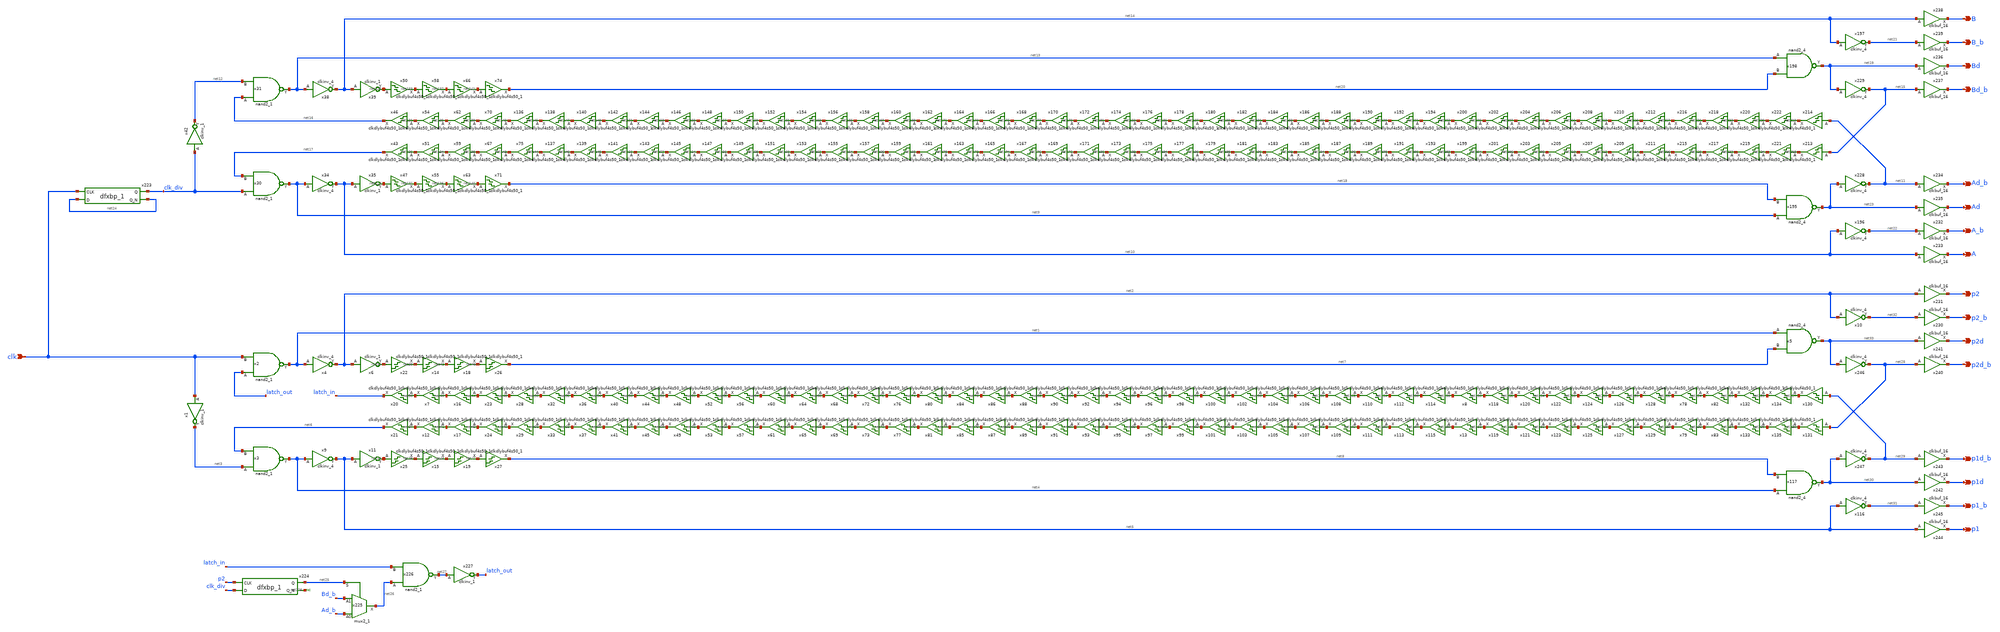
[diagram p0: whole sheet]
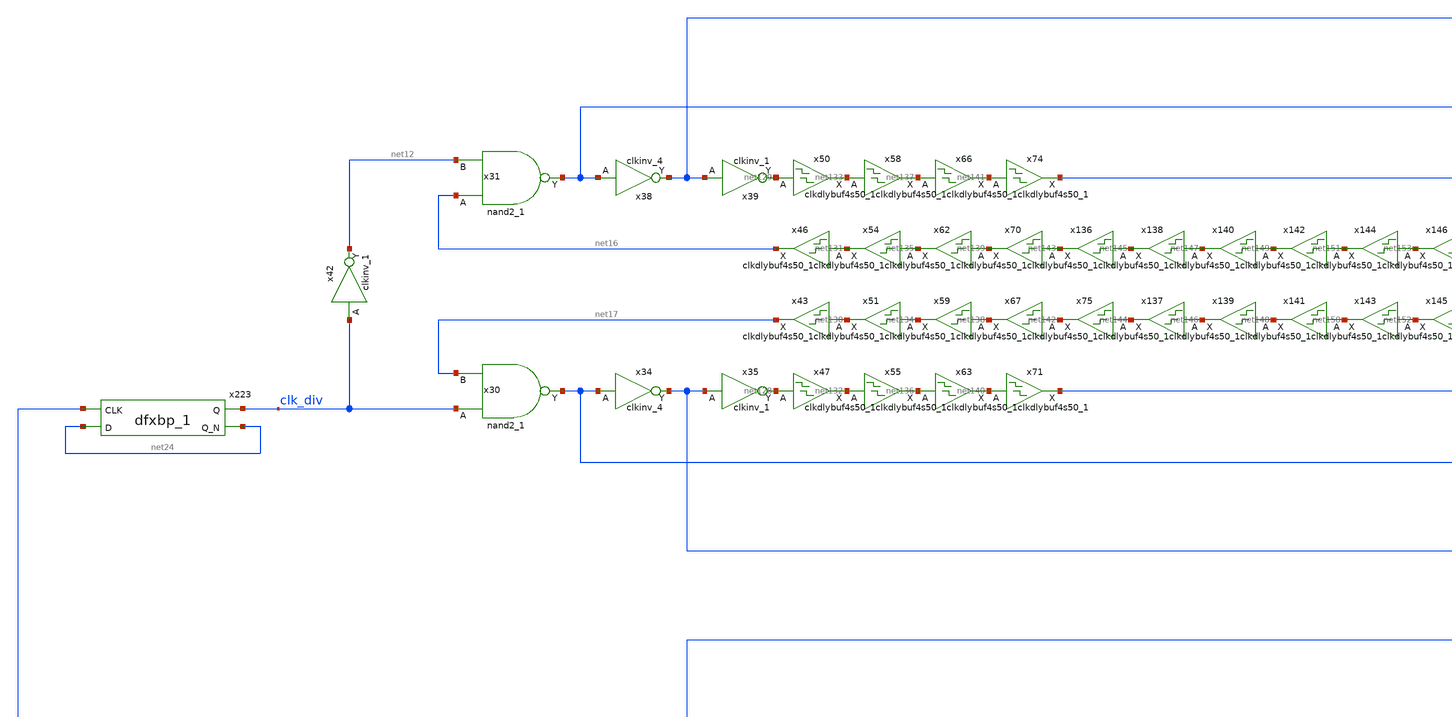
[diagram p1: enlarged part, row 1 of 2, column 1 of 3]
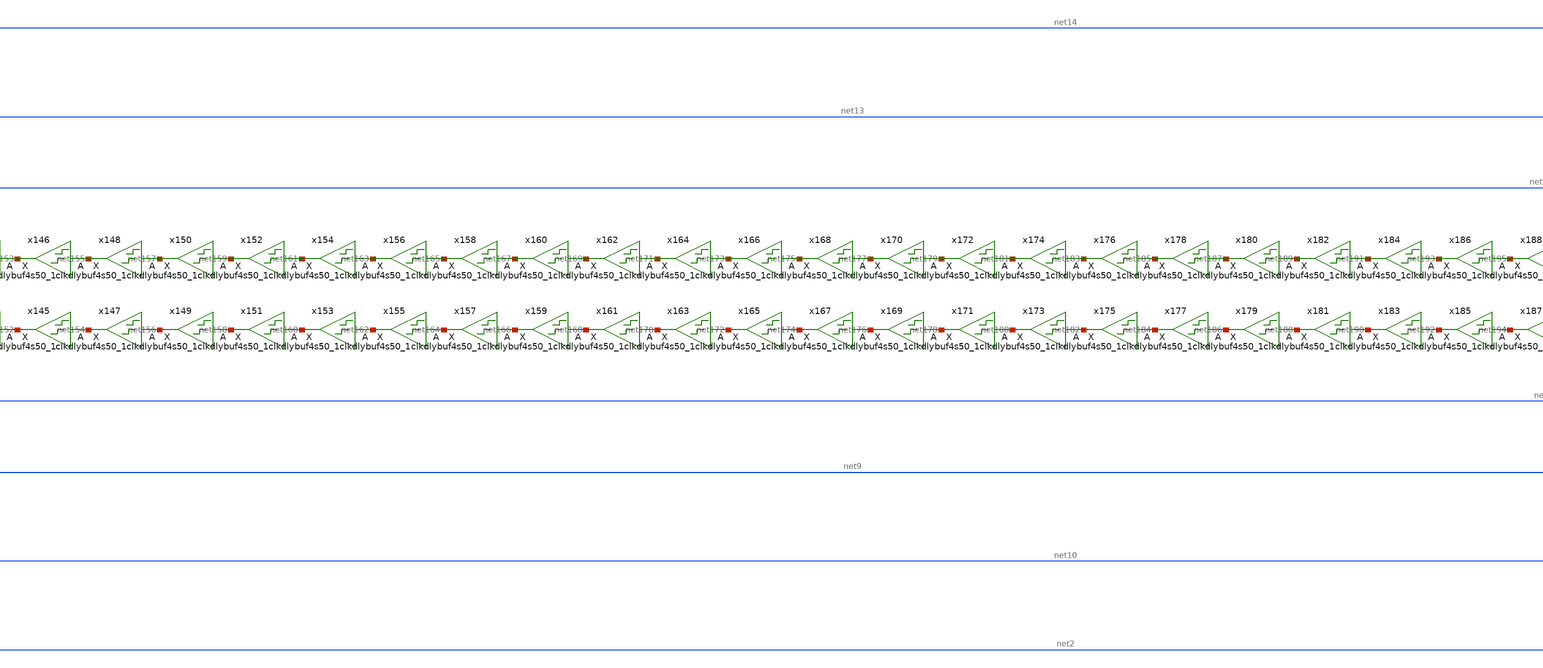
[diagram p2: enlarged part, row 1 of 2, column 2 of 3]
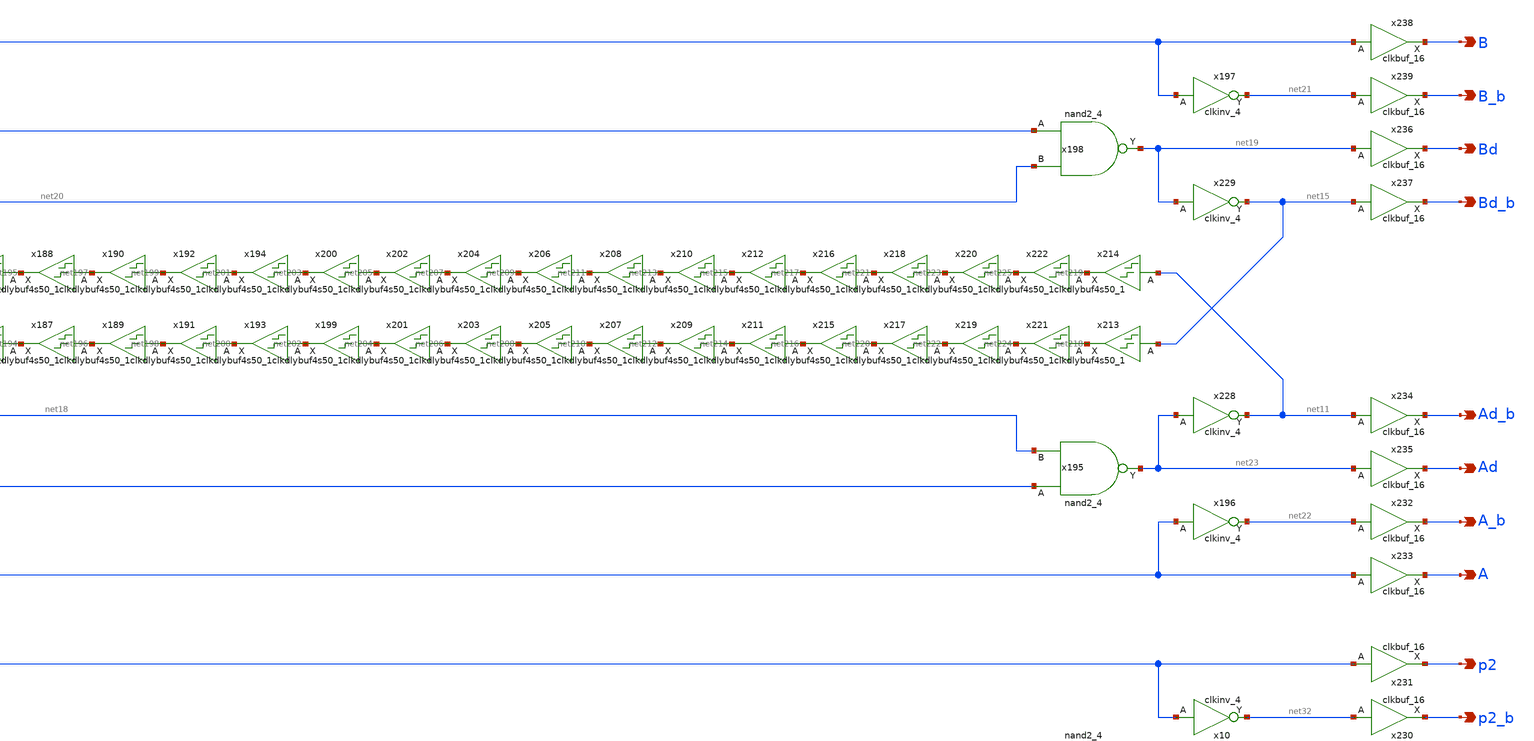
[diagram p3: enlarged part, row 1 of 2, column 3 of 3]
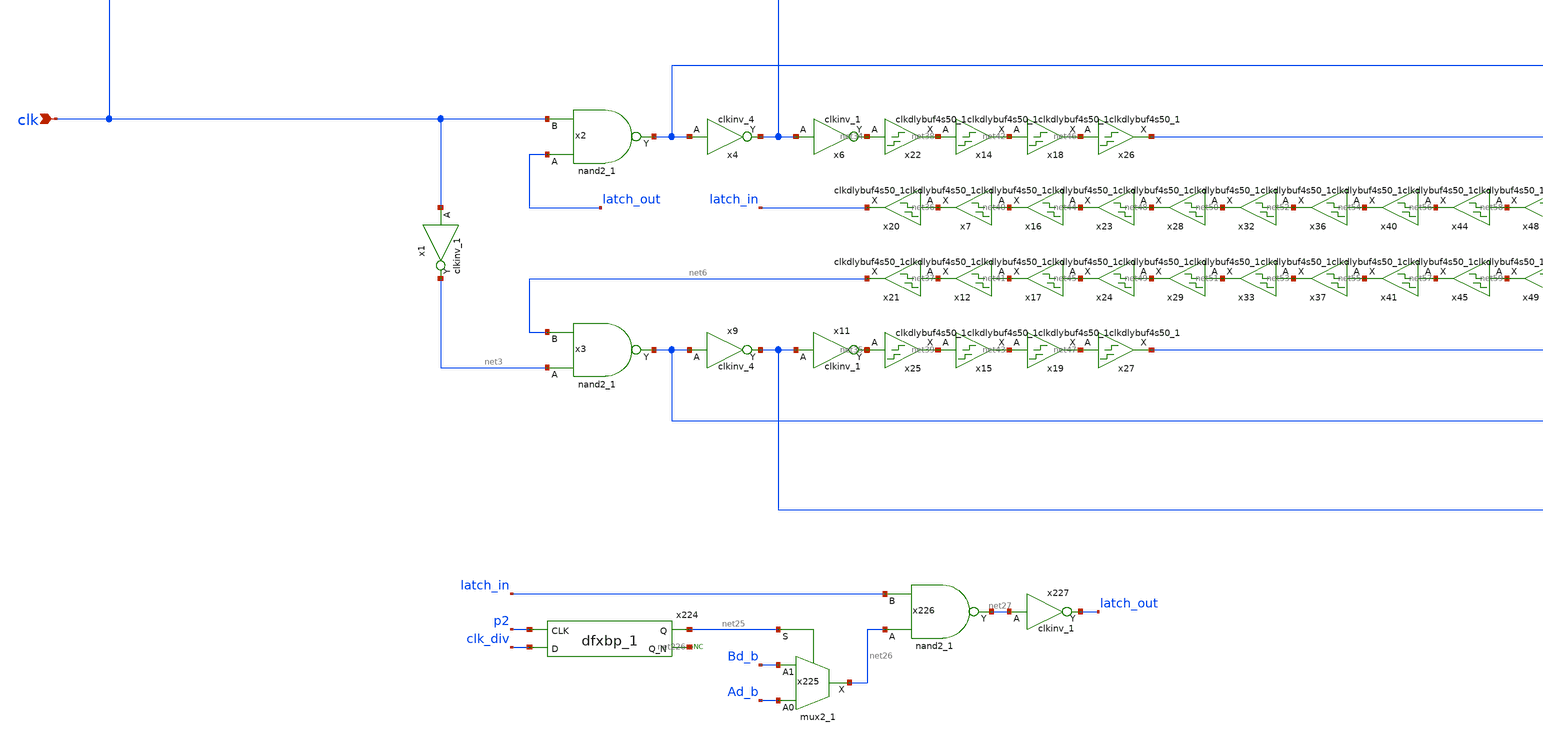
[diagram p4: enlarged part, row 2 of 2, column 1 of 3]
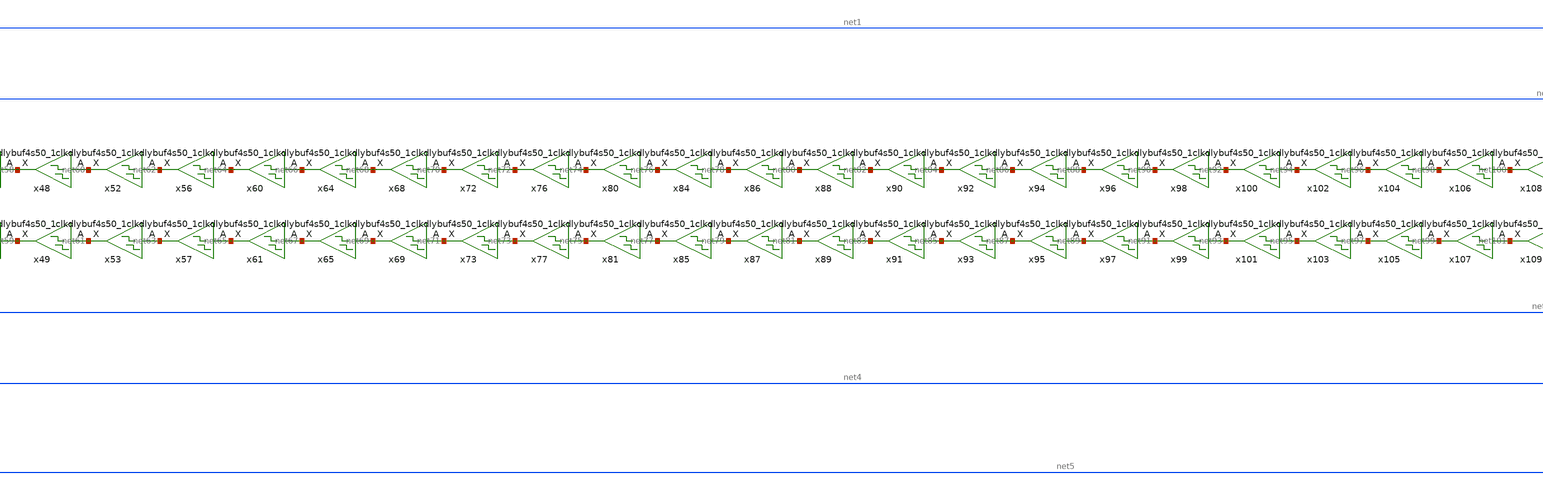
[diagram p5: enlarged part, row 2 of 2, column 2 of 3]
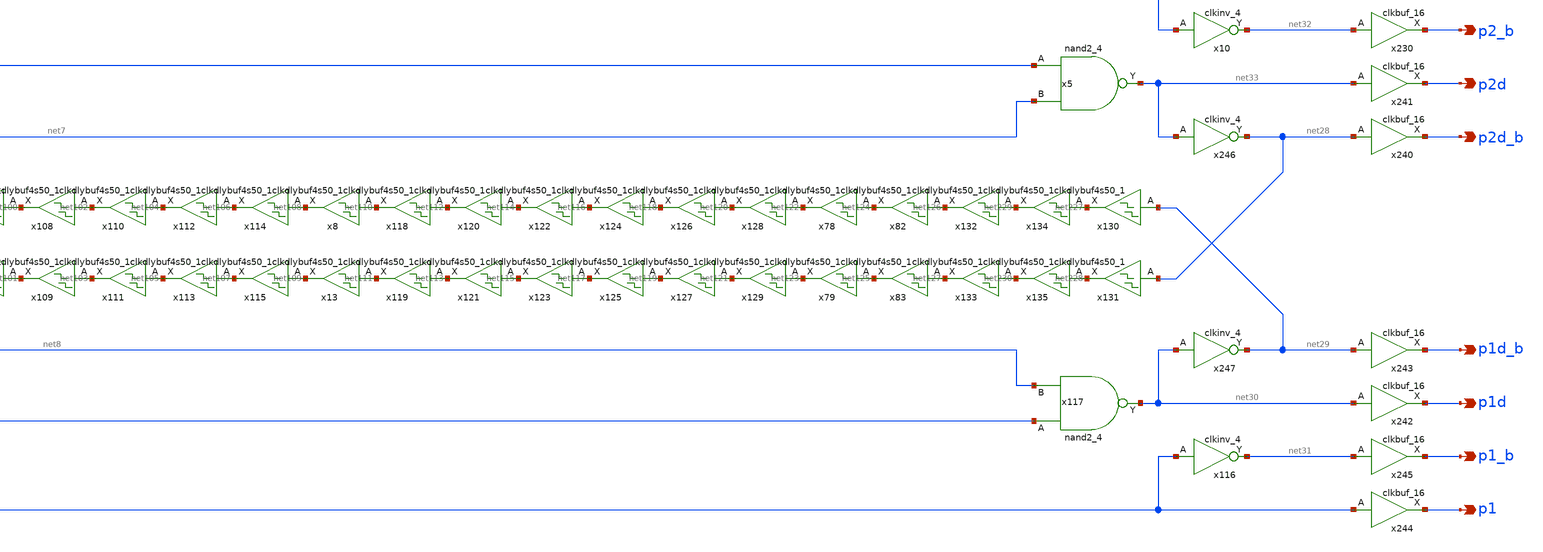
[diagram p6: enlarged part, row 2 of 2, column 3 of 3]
** sch_path: design/analog_modulator/schematic/clock.sch
**.subckt clock clk p2d_b p2d p2_b p2 p1d_b p1d p1_b p1 Ad_b Ad A_b A Bd_b Bd B_b B
*.ipin clk
*.opin p2d_b
*.opin p2d
*.opin p2_b
*.opin p2
*.opin p1d_b
*.opin p1d
*.opin p1_b
*.opin p1
*.opin Ad_b
*.opin Ad
*.opin A_b
*.opin A
*.opin Bd_b
*.opin Bd
*.opin B_b
*.opin B
x2 latch_out clk VSS VSS VDD VDD net1 sky130_fd_sc_hd__nand2_1
x3 net3 net6 VSS VSS VDD VDD net4 sky130_fd_sc_hd__nand2_1
x4 net1 VSS VSS VDD VDD net2 sky130_fd_sc_hd__clkinv_4
x6 net2 VSS VSS VDD VDD net34 sky130_fd_sc_hd__clkinv_1
x9 net4 VSS VSS VDD VDD net5 sky130_fd_sc_hd__clkinv_4
x11 net5 VSS VSS VDD VDD net35 sky130_fd_sc_hd__clkinv_1
x1 clk VSS VSS VDD VDD net3 sky130_fd_sc_hd__clkinv_1
x20 net36 VSS VSS VDD VDD latch_in sky130_fd_sc_hd__clkdlybuf4s50_1
x21 net37 VSS VSS VDD VDD net6 sky130_fd_sc_hd__clkdlybuf4s50_1
x22 net34 VSS VSS VDD VDD net38 sky130_fd_sc_hd__clkdlybuf4s50_1
x25 net35 VSS VSS VDD VDD net39 sky130_fd_sc_hd__clkdlybuf4s50_1
x7 net40 VSS VSS VDD VDD net36 sky130_fd_sc_hd__clkdlybuf4s50_1
x12 net41 VSS VSS VDD VDD net37 sky130_fd_sc_hd__clkdlybuf4s50_1
x14 net38 VSS VSS VDD VDD net42 sky130_fd_sc_hd__clkdlybuf4s50_1
x15 net39 VSS VSS VDD VDD net43 sky130_fd_sc_hd__clkdlybuf4s50_1
x16 net44 VSS VSS VDD VDD net40 sky130_fd_sc_hd__clkdlybuf4s50_1
x17 net45 VSS VSS VDD VDD net41 sky130_fd_sc_hd__clkdlybuf4s50_1
x18 net42 VSS VSS VDD VDD net46 sky130_fd_sc_hd__clkdlybuf4s50_1
x19 net43 VSS VSS VDD VDD net47 sky130_fd_sc_hd__clkdlybuf4s50_1
x23 net48 VSS VSS VDD VDD net44 sky130_fd_sc_hd__clkdlybuf4s50_1
x24 net49 VSS VSS VDD VDD net45 sky130_fd_sc_hd__clkdlybuf4s50_1
x26 net46 VSS VSS VDD VDD net7 sky130_fd_sc_hd__clkdlybuf4s50_1
x27 net47 VSS VSS VDD VDD net8 sky130_fd_sc_hd__clkdlybuf4s50_1
x28 net50 VSS VSS VDD VDD net48 sky130_fd_sc_hd__clkdlybuf4s50_1
x29 net51 VSS VSS VDD VDD net49 sky130_fd_sc_hd__clkdlybuf4s50_1
x32 net52 VSS VSS VDD VDD net50 sky130_fd_sc_hd__clkdlybuf4s50_1
x33 net53 VSS VSS VDD VDD net51 sky130_fd_sc_hd__clkdlybuf4s50_1
x36 net54 VSS VSS VDD VDD net52 sky130_fd_sc_hd__clkdlybuf4s50_1
x37 net55 VSS VSS VDD VDD net53 sky130_fd_sc_hd__clkdlybuf4s50_1
x40 net56 VSS VSS VDD VDD net54 sky130_fd_sc_hd__clkdlybuf4s50_1
x41 net57 VSS VSS VDD VDD net55 sky130_fd_sc_hd__clkdlybuf4s50_1
x44 net58 VSS VSS VDD VDD net56 sky130_fd_sc_hd__clkdlybuf4s50_1
x45 net59 VSS VSS VDD VDD net57 sky130_fd_sc_hd__clkdlybuf4s50_1
x48 net60 VSS VSS VDD VDD net58 sky130_fd_sc_hd__clkdlybuf4s50_1
x49 net61 VSS VSS VDD VDD net59 sky130_fd_sc_hd__clkdlybuf4s50_1
x52 net62 VSS VSS VDD VDD net60 sky130_fd_sc_hd__clkdlybuf4s50_1
x53 net63 VSS VSS VDD VDD net61 sky130_fd_sc_hd__clkdlybuf4s50_1
x56 net64 VSS VSS VDD VDD net62 sky130_fd_sc_hd__clkdlybuf4s50_1
x57 net65 VSS VSS VDD VDD net63 sky130_fd_sc_hd__clkdlybuf4s50_1
x60 net66 VSS VSS VDD VDD net64 sky130_fd_sc_hd__clkdlybuf4s50_1
x61 net67 VSS VSS VDD VDD net65 sky130_fd_sc_hd__clkdlybuf4s50_1
x64 net68 VSS VSS VDD VDD net66 sky130_fd_sc_hd__clkdlybuf4s50_1
x65 net69 VSS VSS VDD VDD net67 sky130_fd_sc_hd__clkdlybuf4s50_1
x68 net70 VSS VSS VDD VDD net68 sky130_fd_sc_hd__clkdlybuf4s50_1
x69 net71 VSS VSS VDD VDD net69 sky130_fd_sc_hd__clkdlybuf4s50_1
x72 net72 VSS VSS VDD VDD net70 sky130_fd_sc_hd__clkdlybuf4s50_1
x73 net73 VSS VSS VDD VDD net71 sky130_fd_sc_hd__clkdlybuf4s50_1
x76 net74 VSS VSS VDD VDD net72 sky130_fd_sc_hd__clkdlybuf4s50_1
x77 net75 VSS VSS VDD VDD net73 sky130_fd_sc_hd__clkdlybuf4s50_1
x80 net76 VSS VSS VDD VDD net74 sky130_fd_sc_hd__clkdlybuf4s50_1
x81 net77 VSS VSS VDD VDD net75 sky130_fd_sc_hd__clkdlybuf4s50_1
x84 net78 VSS VSS VDD VDD net76 sky130_fd_sc_hd__clkdlybuf4s50_1
x85 net79 VSS VSS VDD VDD net77 sky130_fd_sc_hd__clkdlybuf4s50_1
x86 net80 VSS VSS VDD VDD net78 sky130_fd_sc_hd__clkdlybuf4s50_1
x87 net81 VSS VSS VDD VDD net79 sky130_fd_sc_hd__clkdlybuf4s50_1
x88 net82 VSS VSS VDD VDD net80 sky130_fd_sc_hd__clkdlybuf4s50_1
x89 net83 VSS VSS VDD VDD net81 sky130_fd_sc_hd__clkdlybuf4s50_1
x90 net84 VSS VSS VDD VDD net82 sky130_fd_sc_hd__clkdlybuf4s50_1
x91 net85 VSS VSS VDD VDD net83 sky130_fd_sc_hd__clkdlybuf4s50_1
x92 net86 VSS VSS VDD VDD net84 sky130_fd_sc_hd__clkdlybuf4s50_1
x93 net87 VSS VSS VDD VDD net85 sky130_fd_sc_hd__clkdlybuf4s50_1
x94 net88 VSS VSS VDD VDD net86 sky130_fd_sc_hd__clkdlybuf4s50_1
x95 net89 VSS VSS VDD VDD net87 sky130_fd_sc_hd__clkdlybuf4s50_1
x96 net90 VSS VSS VDD VDD net88 sky130_fd_sc_hd__clkdlybuf4s50_1
x97 net91 VSS VSS VDD VDD net89 sky130_fd_sc_hd__clkdlybuf4s50_1
x98 net92 VSS VSS VDD VDD net90 sky130_fd_sc_hd__clkdlybuf4s50_1
x99 net93 VSS VSS VDD VDD net91 sky130_fd_sc_hd__clkdlybuf4s50_1
x100 net94 VSS VSS VDD VDD net92 sky130_fd_sc_hd__clkdlybuf4s50_1
x101 net95 VSS VSS VDD VDD net93 sky130_fd_sc_hd__clkdlybuf4s50_1
x102 net96 VSS VSS VDD VDD net94 sky130_fd_sc_hd__clkdlybuf4s50_1
x103 net97 VSS VSS VDD VDD net95 sky130_fd_sc_hd__clkdlybuf4s50_1
x104 net98 VSS VSS VDD VDD net96 sky130_fd_sc_hd__clkdlybuf4s50_1
x105 net99 VSS VSS VDD VDD net97 sky130_fd_sc_hd__clkdlybuf4s50_1
x106 net100 VSS VSS VDD VDD net98 sky130_fd_sc_hd__clkdlybuf4s50_1
x107 net101 VSS VSS VDD VDD net99 sky130_fd_sc_hd__clkdlybuf4s50_1
x108 net102 VSS VSS VDD VDD net100 sky130_fd_sc_hd__clkdlybuf4s50_1
x109 net103 VSS VSS VDD VDD net101 sky130_fd_sc_hd__clkdlybuf4s50_1
x110 net104 VSS VSS VDD VDD net102 sky130_fd_sc_hd__clkdlybuf4s50_1
x111 net105 VSS VSS VDD VDD net103 sky130_fd_sc_hd__clkdlybuf4s50_1
x112 net106 VSS VSS VDD VDD net104 sky130_fd_sc_hd__clkdlybuf4s50_1
x113 net107 VSS VSS VDD VDD net105 sky130_fd_sc_hd__clkdlybuf4s50_1
x114 net108 VSS VSS VDD VDD net106 sky130_fd_sc_hd__clkdlybuf4s50_1
x115 net109 VSS VSS VDD VDD net107 sky130_fd_sc_hd__clkdlybuf4s50_1
x8 net110 VSS VSS VDD VDD net108 sky130_fd_sc_hd__clkdlybuf4s50_1
x13 net111 VSS VSS VDD VDD net109 sky130_fd_sc_hd__clkdlybuf4s50_1
x118 net112 VSS VSS VDD VDD net110 sky130_fd_sc_hd__clkdlybuf4s50_1
x119 net113 VSS VSS VDD VDD net111 sky130_fd_sc_hd__clkdlybuf4s50_1
x120 net114 VSS VSS VDD VDD net112 sky130_fd_sc_hd__clkdlybuf4s50_1
x121 net115 VSS VSS VDD VDD net113 sky130_fd_sc_hd__clkdlybuf4s50_1
x122 net116 VSS VSS VDD VDD net114 sky130_fd_sc_hd__clkdlybuf4s50_1
x123 net117 VSS VSS VDD VDD net115 sky130_fd_sc_hd__clkdlybuf4s50_1
x124 net118 VSS VSS VDD VDD net116 sky130_fd_sc_hd__clkdlybuf4s50_1
x125 net119 VSS VSS VDD VDD net117 sky130_fd_sc_hd__clkdlybuf4s50_1
x126 net120 VSS VSS VDD VDD net118 sky130_fd_sc_hd__clkdlybuf4s50_1
x127 net121 VSS VSS VDD VDD net119 sky130_fd_sc_hd__clkdlybuf4s50_1
x128 net122 VSS VSS VDD VDD net120 sky130_fd_sc_hd__clkdlybuf4s50_1
x129 net123 VSS VSS VDD VDD net121 sky130_fd_sc_hd__clkdlybuf4s50_1
x78 net124 VSS VSS VDD VDD net122 sky130_fd_sc_hd__clkdlybuf4s50_1
x79 net125 VSS VSS VDD VDD net123 sky130_fd_sc_hd__clkdlybuf4s50_1
x82 net126 VSS VSS VDD VDD net124 sky130_fd_sc_hd__clkdlybuf4s50_1
x83 net127 VSS VSS VDD VDD net125 sky130_fd_sc_hd__clkdlybuf4s50_1
x30 clk_div net17 VSS VSS VDD VDD net9 sky130_fd_sc_hd__nand2_1
x31 net16 net12 VSS VSS VDD VDD net13 sky130_fd_sc_hd__nand2_1
x34 net9 VSS VSS VDD VDD net10 sky130_fd_sc_hd__clkinv_4
x35 net10 VSS VSS VDD VDD net128 sky130_fd_sc_hd__clkinv_1
x38 net13 VSS VSS VDD VDD net14 sky130_fd_sc_hd__clkinv_4
x39 net14 VSS VSS VDD VDD net129 sky130_fd_sc_hd__clkinv_1
x42 clk_div VSS VSS VDD VDD net12 sky130_fd_sc_hd__clkinv_1
x43 net130 VSS VSS VDD VDD net17 sky130_fd_sc_hd__clkdlybuf4s50_1
x46 net131 VSS VSS VDD VDD net16 sky130_fd_sc_hd__clkdlybuf4s50_1
x47 net128 VSS VSS VDD VDD net132 sky130_fd_sc_hd__clkdlybuf4s50_1
x50 net129 VSS VSS VDD VDD net133 sky130_fd_sc_hd__clkdlybuf4s50_1
x51 net134 VSS VSS VDD VDD net130 sky130_fd_sc_hd__clkdlybuf4s50_1
x54 net135 VSS VSS VDD VDD net131 sky130_fd_sc_hd__clkdlybuf4s50_1
x55 net132 VSS VSS VDD VDD net136 sky130_fd_sc_hd__clkdlybuf4s50_1
x58 net133 VSS VSS VDD VDD net137 sky130_fd_sc_hd__clkdlybuf4s50_1
x59 net138 VSS VSS VDD VDD net134 sky130_fd_sc_hd__clkdlybuf4s50_1
x62 net139 VSS VSS VDD VDD net135 sky130_fd_sc_hd__clkdlybuf4s50_1
x63 net136 VSS VSS VDD VDD net140 sky130_fd_sc_hd__clkdlybuf4s50_1
x66 net137 VSS VSS VDD VDD net141 sky130_fd_sc_hd__clkdlybuf4s50_1
x67 net142 VSS VSS VDD VDD net138 sky130_fd_sc_hd__clkdlybuf4s50_1
x70 net143 VSS VSS VDD VDD net139 sky130_fd_sc_hd__clkdlybuf4s50_1
x71 net140 VSS VSS VDD VDD net18 sky130_fd_sc_hd__clkdlybuf4s50_1
x74 net141 VSS VSS VDD VDD net20 sky130_fd_sc_hd__clkdlybuf4s50_1
x75 net144 VSS VSS VDD VDD net142 sky130_fd_sc_hd__clkdlybuf4s50_1
x136 net145 VSS VSS VDD VDD net143 sky130_fd_sc_hd__clkdlybuf4s50_1
x137 net146 VSS VSS VDD VDD net144 sky130_fd_sc_hd__clkdlybuf4s50_1
x138 net147 VSS VSS VDD VDD net145 sky130_fd_sc_hd__clkdlybuf4s50_1
x139 net148 VSS VSS VDD VDD net146 sky130_fd_sc_hd__clkdlybuf4s50_1
x140 net149 VSS VSS VDD VDD net147 sky130_fd_sc_hd__clkdlybuf4s50_1
x141 net150 VSS VSS VDD VDD net148 sky130_fd_sc_hd__clkdlybuf4s50_1
x142 net151 VSS VSS VDD VDD net149 sky130_fd_sc_hd__clkdlybuf4s50_1
x143 net152 VSS VSS VDD VDD net150 sky130_fd_sc_hd__clkdlybuf4s50_1
x144 net153 VSS VSS VDD VDD net151 sky130_fd_sc_hd__clkdlybuf4s50_1
x145 net154 VSS VSS VDD VDD net152 sky130_fd_sc_hd__clkdlybuf4s50_1
x146 net155 VSS VSS VDD VDD net153 sky130_fd_sc_hd__clkdlybuf4s50_1
x147 net156 VSS VSS VDD VDD net154 sky130_fd_sc_hd__clkdlybuf4s50_1
x148 net157 VSS VSS VDD VDD net155 sky130_fd_sc_hd__clkdlybuf4s50_1
x149 net158 VSS VSS VDD VDD net156 sky130_fd_sc_hd__clkdlybuf4s50_1
x150 net159 VSS VSS VDD VDD net157 sky130_fd_sc_hd__clkdlybuf4s50_1
x151 net160 VSS VSS VDD VDD net158 sky130_fd_sc_hd__clkdlybuf4s50_1
x152 net161 VSS VSS VDD VDD net159 sky130_fd_sc_hd__clkdlybuf4s50_1
x153 net162 VSS VSS VDD VDD net160 sky130_fd_sc_hd__clkdlybuf4s50_1
x154 net163 VSS VSS VDD VDD net161 sky130_fd_sc_hd__clkdlybuf4s50_1
x155 net164 VSS VSS VDD VDD net162 sky130_fd_sc_hd__clkdlybuf4s50_1
x156 net165 VSS VSS VDD VDD net163 sky130_fd_sc_hd__clkdlybuf4s50_1
x157 net166 VSS VSS VDD VDD net164 sky130_fd_sc_hd__clkdlybuf4s50_1
x158 net167 VSS VSS VDD VDD net165 sky130_fd_sc_hd__clkdlybuf4s50_1
x159 net168 VSS VSS VDD VDD net166 sky130_fd_sc_hd__clkdlybuf4s50_1
x160 net169 VSS VSS VDD VDD net167 sky130_fd_sc_hd__clkdlybuf4s50_1
x161 net170 VSS VSS VDD VDD net168 sky130_fd_sc_hd__clkdlybuf4s50_1
x162 net171 VSS VSS VDD VDD net169 sky130_fd_sc_hd__clkdlybuf4s50_1
x163 net172 VSS VSS VDD VDD net170 sky130_fd_sc_hd__clkdlybuf4s50_1
x164 net173 VSS VSS VDD VDD net171 sky130_fd_sc_hd__clkdlybuf4s50_1
x165 net174 VSS VSS VDD VDD net172 sky130_fd_sc_hd__clkdlybuf4s50_1
x166 net175 VSS VSS VDD VDD net173 sky130_fd_sc_hd__clkdlybuf4s50_1
x167 net176 VSS VSS VDD VDD net174 sky130_fd_sc_hd__clkdlybuf4s50_1
x168 net177 VSS VSS VDD VDD net175 sky130_fd_sc_hd__clkdlybuf4s50_1
x169 net178 VSS VSS VDD VDD net176 sky130_fd_sc_hd__clkdlybuf4s50_1
x170 net179 VSS VSS VDD VDD net177 sky130_fd_sc_hd__clkdlybuf4s50_1
x171 net180 VSS VSS VDD VDD net178 sky130_fd_sc_hd__clkdlybuf4s50_1
x172 net181 VSS VSS VDD VDD net179 sky130_fd_sc_hd__clkdlybuf4s50_1
x173 net182 VSS VSS VDD VDD net180 sky130_fd_sc_hd__clkdlybuf4s50_1
x174 net183 VSS VSS VDD VDD net181 sky130_fd_sc_hd__clkdlybuf4s50_1
x175 net184 VSS VSS VDD VDD net182 sky130_fd_sc_hd__clkdlybuf4s50_1
x176 net185 VSS VSS VDD VDD net183 sky130_fd_sc_hd__clkdlybuf4s50_1
x177 net186 VSS VSS VDD VDD net184 sky130_fd_sc_hd__clkdlybuf4s50_1
x178 net187 VSS VSS VDD VDD net185 sky130_fd_sc_hd__clkdlybuf4s50_1
x179 net188 VSS VSS VDD VDD net186 sky130_fd_sc_hd__clkdlybuf4s50_1
x180 net189 VSS VSS VDD VDD net187 sky130_fd_sc_hd__clkdlybuf4s50_1
x181 net190 VSS VSS VDD VDD net188 sky130_fd_sc_hd__clkdlybuf4s50_1
x182 net191 VSS VSS VDD VDD net189 sky130_fd_sc_hd__clkdlybuf4s50_1
x183 net192 VSS VSS VDD VDD net190 sky130_fd_sc_hd__clkdlybuf4s50_1
x184 net193 VSS VSS VDD VDD net191 sky130_fd_sc_hd__clkdlybuf4s50_1
x185 net194 VSS VSS VDD VDD net192 sky130_fd_sc_hd__clkdlybuf4s50_1
x186 net195 VSS VSS VDD VDD net193 sky130_fd_sc_hd__clkdlybuf4s50_1
x187 net196 VSS VSS VDD VDD net194 sky130_fd_sc_hd__clkdlybuf4s50_1
x188 net197 VSS VSS VDD VDD net195 sky130_fd_sc_hd__clkdlybuf4s50_1
x189 net198 VSS VSS VDD VDD net196 sky130_fd_sc_hd__clkdlybuf4s50_1
x190 net199 VSS VSS VDD VDD net197 sky130_fd_sc_hd__clkdlybuf4s50_1
x191 net200 VSS VSS VDD VDD net198 sky130_fd_sc_hd__clkdlybuf4s50_1
x192 net201 VSS VSS VDD VDD net199 sky130_fd_sc_hd__clkdlybuf4s50_1
x193 net202 VSS VSS VDD VDD net200 sky130_fd_sc_hd__clkdlybuf4s50_1
x194 net203 VSS VSS VDD VDD net201 sky130_fd_sc_hd__clkdlybuf4s50_1
x195 net9 net18 VSS VSS VDD VDD net23 sky130_fd_sc_hd__nand2_4
x196 net10 VSS VSS VDD VDD net22 sky130_fd_sc_hd__clkinv_4
x197 net14 VSS VSS VDD VDD net21 sky130_fd_sc_hd__clkinv_4
x198 net13 net20 VSS VSS VDD VDD net19 sky130_fd_sc_hd__nand2_4
x199 net204 VSS VSS VDD VDD net202 sky130_fd_sc_hd__clkdlybuf4s50_1
x200 net205 VSS VSS VDD VDD net203 sky130_fd_sc_hd__clkdlybuf4s50_1
x201 net206 VSS VSS VDD VDD net204 sky130_fd_sc_hd__clkdlybuf4s50_1
x202 net207 VSS VSS VDD VDD net205 sky130_fd_sc_hd__clkdlybuf4s50_1
x203 net208 VSS VSS VDD VDD net206 sky130_fd_sc_hd__clkdlybuf4s50_1
x204 net209 VSS VSS VDD VDD net207 sky130_fd_sc_hd__clkdlybuf4s50_1
x205 net210 VSS VSS VDD VDD net208 sky130_fd_sc_hd__clkdlybuf4s50_1
x206 net211 VSS VSS VDD VDD net209 sky130_fd_sc_hd__clkdlybuf4s50_1
x207 net212 VSS VSS VDD VDD net210 sky130_fd_sc_hd__clkdlybuf4s50_1
x208 net213 VSS VSS VDD VDD net211 sky130_fd_sc_hd__clkdlybuf4s50_1
x209 net214 VSS VSS VDD VDD net212 sky130_fd_sc_hd__clkdlybuf4s50_1
x210 net215 VSS VSS VDD VDD net213 sky130_fd_sc_hd__clkdlybuf4s50_1
x211 net216 VSS VSS VDD VDD net214 sky130_fd_sc_hd__clkdlybuf4s50_1
x212 net217 VSS VSS VDD VDD net215 sky130_fd_sc_hd__clkdlybuf4s50_1
x213 net15 VSS VSS VDD VDD net218 sky130_fd_sc_hd__clkdlybuf4s50_1
x214 net11 VSS VSS VDD VDD net219 sky130_fd_sc_hd__clkdlybuf4s50_1
x215 net220 VSS VSS VDD VDD net216 sky130_fd_sc_hd__clkdlybuf4s50_1
x216 net221 VSS VSS VDD VDD net217 sky130_fd_sc_hd__clkdlybuf4s50_1
x217 net222 VSS VSS VDD VDD net220 sky130_fd_sc_hd__clkdlybuf4s50_1
x218 net223 VSS VSS VDD VDD net221 sky130_fd_sc_hd__clkdlybuf4s50_1
x219 net224 VSS VSS VDD VDD net222 sky130_fd_sc_hd__clkdlybuf4s50_1
x220 net225 VSS VSS VDD VDD net223 sky130_fd_sc_hd__clkdlybuf4s50_1
x221 net218 VSS VSS VDD VDD net224 sky130_fd_sc_hd__clkdlybuf4s50_1
x222 net219 VSS VSS VDD VDD net225 sky130_fd_sc_hd__clkdlybuf4s50_1
x223 clk net24 VSS VSS VDD VDD clk_div net24 sky130_fd_sc_hd__dfxbp_1
x224 p2 clk_div VSS VSS VDD VDD net25 net226 sky130_fd_sc_hd__dfxbp_1
x225 Ad_b Bd_b net25 VSS VSS VDD VDD net26 sky130_fd_sc_hd__mux2_1
x226 net26 latch_in VSS VSS VDD VDD net27 sky130_fd_sc_hd__nand2_1
x227 net27 VSS VSS VDD VDD latch_out sky130_fd_sc_hd__clkinv_1
* noconn #net226
x232 net22 VSS VSS VDD VDD A_b sky130_fd_sc_hd__clkbuf_16
x233 net10 VSS VSS VDD VDD A sky130_fd_sc_hd__clkbuf_16
x234 net11 VSS VSS VDD VDD Ad_b sky130_fd_sc_hd__clkbuf_16
x235 net23 VSS VSS VDD VDD Ad sky130_fd_sc_hd__clkbuf_16
x236 net19 VSS VSS VDD VDD Bd sky130_fd_sc_hd__clkbuf_16
x237 net15 VSS VSS VDD VDD Bd_b sky130_fd_sc_hd__clkbuf_16
x238 net14 VSS VSS VDD VDD B sky130_fd_sc_hd__clkbuf_16
x239 net21 VSS VSS VDD VDD B_b sky130_fd_sc_hd__clkbuf_16
x228 net23 VSS VSS VDD VDD net11 sky130_fd_sc_hd__clkinv_4
x229 net19 VSS VSS VDD VDD net15 sky130_fd_sc_hd__clkinv_4
x5 net1 net7 VSS VSS VDD VDD net33 sky130_fd_sc_hd__nand2_4
x10 net2 VSS VSS VDD VDD net32 sky130_fd_sc_hd__clkinv_4
x116 net5 VSS VSS VDD VDD net31 sky130_fd_sc_hd__clkinv_4
x117 net4 net8 VSS VSS VDD VDD net30 sky130_fd_sc_hd__nand2_4
x130 net29 VSS VSS VDD VDD net227 sky130_fd_sc_hd__clkdlybuf4s50_1
x131 net28 VSS VSS VDD VDD net228 sky130_fd_sc_hd__clkdlybuf4s50_1
x132 net229 VSS VSS VDD VDD net126 sky130_fd_sc_hd__clkdlybuf4s50_1
x133 net230 VSS VSS VDD VDD net127 sky130_fd_sc_hd__clkdlybuf4s50_1
x134 net227 VSS VSS VDD VDD net229 sky130_fd_sc_hd__clkdlybuf4s50_1
x135 net228 VSS VSS VDD VDD net230 sky130_fd_sc_hd__clkdlybuf4s50_1
x230 net32 VSS VSS VDD VDD p2_b sky130_fd_sc_hd__clkbuf_16
x231 net2 VSS VSS VDD VDD p2 sky130_fd_sc_hd__clkbuf_16
x240 net28 VSS VSS VDD VDD p2d_b sky130_fd_sc_hd__clkbuf_16
x241 net33 VSS VSS VDD VDD p2d sky130_fd_sc_hd__clkbuf_16
x242 net30 VSS VSS VDD VDD p1d sky130_fd_sc_hd__clkbuf_16
x243 net29 VSS VSS VDD VDD p1d_b sky130_fd_sc_hd__clkbuf_16
x244 net5 VSS VSS VDD VDD p1 sky130_fd_sc_hd__clkbuf_16
x245 net31 VSS VSS VDD VDD p1_b sky130_fd_sc_hd__clkbuf_16
x246 net33 VSS VSS VDD VDD net28 sky130_fd_sc_hd__clkinv_4
x247 net30 VSS VSS VDD VDD net29 sky130_fd_sc_hd__clkinv_4
**.ends
.end
